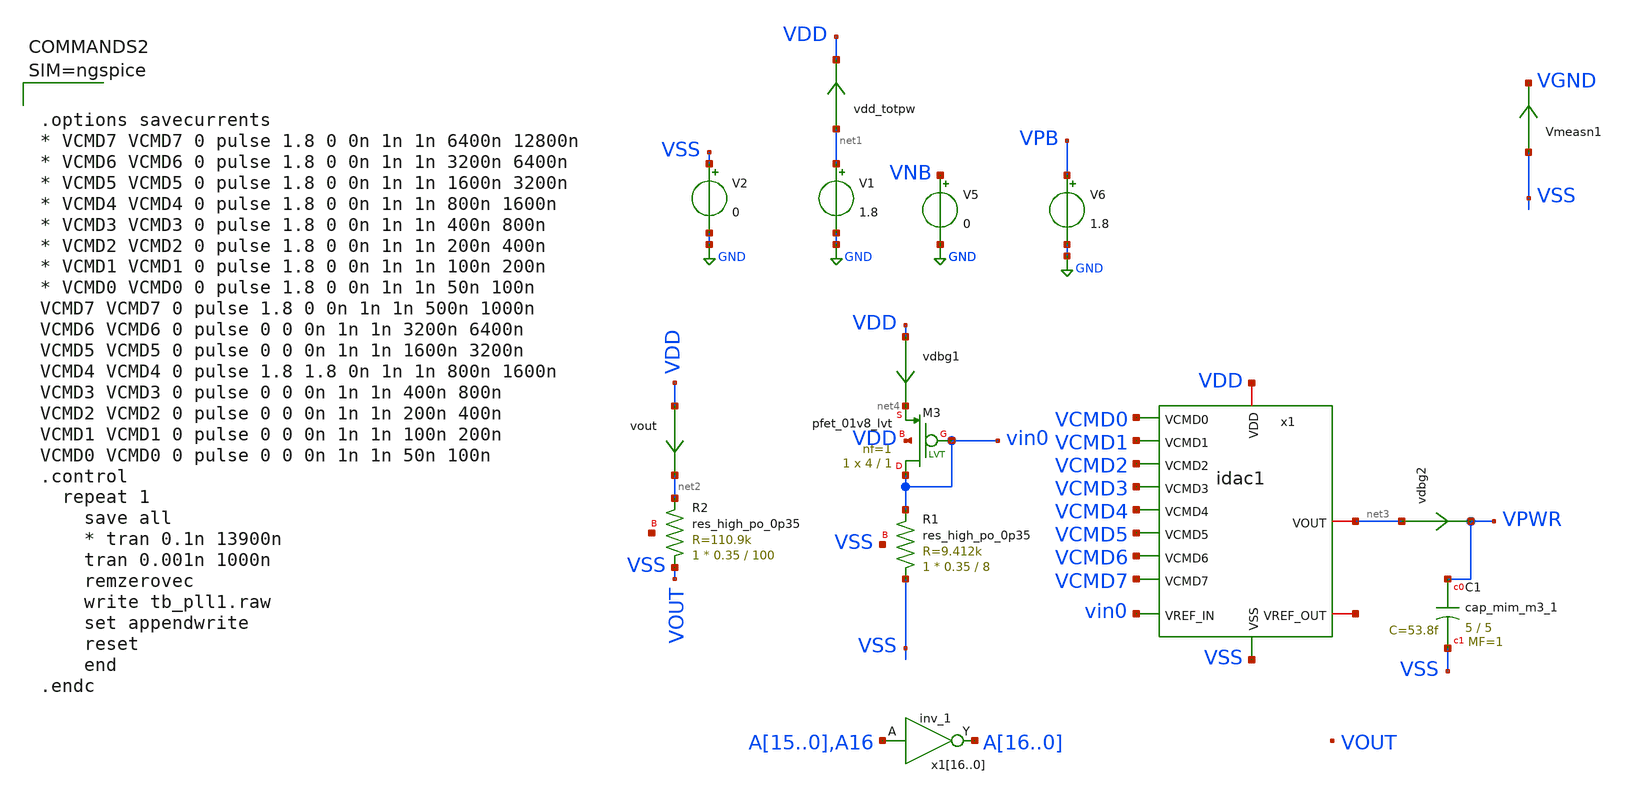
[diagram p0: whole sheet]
** sch_path: xschem/tb_pll1.sch
**.subckt tb_pll1
V5 VNB GND 0
V6 VPB GND 1.8
V1 net1 GND 1.8
V2 VSS GND 0
XM3 vin0 vin0 net4 VDD sky130_fd_pr__pfet_01v8_lvt L=1 W=4 nf=1 ad='int((nf+1)/2) * W/nf * 0.29' as='int((nf+2)/2) * W/nf * 0.29'
+ pd='2*int((nf+1)/2) * (W/nf + 0.29)' ps='2*int((nf+2)/2) * (W/nf + 0.29)' nrd='0.29 / W' nrs='0.29 / W'
+ sa=0 sb=0 sd=0 mult=1 m=1
vout VDD net2 0
.save i(vout)
XR1 VSS vin0 VSS sky130_fd_pr__res_high_po_0p35 L=8 mult=1 m=1
vdbg1 VDD net4 0
.save i(vdbg1)
XR2 VOUT net2 net5 sky130_fd_pr__res_high_po_0p35 L=100 mult=1 m=1
vdd_totpw net1 VDD 0
.save i(vdd_totpw)
x1 VCMD0 VCMD1 VCMD2 VCMD3 VCMD4 VCMD5 VCMD6 VCMD7 VDD net3 vin0 VSS net6 idac1
x116 A15 VGND VNB VPB VPWR A16 sky130_fd_sc_hd__inv_1
x115 A14 VGND VNB VPB VPWR A15 sky130_fd_sc_hd__inv_1
x114 A13 VGND VNB VPB VPWR A14 sky130_fd_sc_hd__inv_1
x113 A12 VGND VNB VPB VPWR A13 sky130_fd_sc_hd__inv_1
x112 A11 VGND VNB VPB VPWR A12 sky130_fd_sc_hd__inv_1
x111 A10 VGND VNB VPB VPWR A11 sky130_fd_sc_hd__inv_1
x110 A9 VGND VNB VPB VPWR A10 sky130_fd_sc_hd__inv_1
x19 A8 VGND VNB VPB VPWR A9 sky130_fd_sc_hd__inv_1
x18 A7 VGND VNB VPB VPWR A8 sky130_fd_sc_hd__inv_1
x17 A6 VGND VNB VPB VPWR A7 sky130_fd_sc_hd__inv_1
x16 A5 VGND VNB VPB VPWR A6 sky130_fd_sc_hd__inv_1
x15 A4 VGND VNB VPB VPWR A5 sky130_fd_sc_hd__inv_1
x14 A3 VGND VNB VPB VPWR A4 sky130_fd_sc_hd__inv_1
x13 A2 VGND VNB VPB VPWR A3 sky130_fd_sc_hd__inv_1
x12 A1 VGND VNB VPB VPWR A2 sky130_fd_sc_hd__inv_1
x11 A0 VGND VNB VPB VPWR A1 sky130_fd_sc_hd__inv_1
x10 A16 VGND VNB VPB VPWR A0 sky130_fd_sc_hd__inv_1
Vmeasn1 VSS VGND 0
.save i(vmeasn1)
vdbg2 net3 VPWR 0
.save i(vdbg2)
XC1 VPWR VSS sky130_fd_pr__cap_mim_m3_1 W=5 L=5 MF=1 m=1
**** begin user architecture code

** opencircuitdesign pdks install
.lib $::SKYWATER_MODELS/sky130.lib.spice tt_mm
*.lib $::SKYWATER_STDCELLS/sky130_fd_sc_hd_blablabla.spice

.subckt sky130_fd_sc_hd__inv_1 A VGND VNB VPB VPWR Y
X0 VGND A Y VNB sky130_fd_pr__nfet_01v8 w=650000u l=150000u
X1 VPWR A Y VPB sky130_fd_pr__pfet_01v8_hvt w=1e+06u l=150000u
.ends





.options savecurrents
* VCMD7 VCMD7 0 pulse 1.8 0 0n 1n 1n 6400n 12800n
* VCMD6 VCMD6 0 pulse 1.8 0 0n 1n 1n 3200n 6400n
* VCMD5 VCMD5 0 pulse 1.8 0 0n 1n 1n 1600n 3200n
* VCMD4 VCMD4 0 pulse 1.8 0 0n 1n 1n 800n 1600n
* VCMD3 VCMD3 0 pulse 1.8 0 0n 1n 1n 400n 800n
* VCMD2 VCMD2 0 pulse 1.8 0 0n 1n 1n 200n 400n
* VCMD1 VCMD1 0 pulse 1.8 0 0n 1n 1n 100n 200n
* VCMD0 VCMD0 0 pulse 1.8 0 0n 1n 1n 50n 100n
VCMD7 VCMD7 0 pulse 1.8 0 0n 1n 1n 500n 1000n
VCMD6 VCMD6 0 pulse 0 0 0n 1n 1n 3200n 6400n
VCMD5 VCMD5 0 pulse 0 0 0n 1n 1n 1600n 3200n
VCMD4 VCMD4 0 pulse 1.8 1.8 0n 1n 1n 800n 1600n
VCMD3 VCMD3 0 pulse 0 0 0n 1n 1n 400n 800n
VCMD2 VCMD2 0 pulse 0 0 0n 1n 1n 200n 400n
VCMD1 VCMD1 0 pulse 0 0 0n 1n 1n 100n 200n
VCMD0 VCMD0 0 pulse 0 0 0n 1n 1n 50n 100n
.control
  repeat 1
    save all
    * tran 0.1n 13900n
    tran 0.001n 1000n
    remzerovec
    write tb_pll1.raw
    set appendwrite
    reset
    end
.endc



**** end user architecture code
**.ends

* expanding   symbol:  idac1.sym # of pins=13
** sym_path: xschem/idac1.sym
** sch_path: xschem/idac1.sch
.subckt idac1 VCMD0 VCMD1 VCMD2 VCMD3 VCMD4 VCMD5 VCMD6 VCMD7 VDD VOUT VREF_IN VSS VREF_OUT
*.ipin VSS
*.iopin VREF_IN
*.iopin VOUT
*.iopin VDD
*.ipin VCMD7
*.ipin VCMD6
*.ipin VCMD5
*.ipin VCMD4
*.ipin VCMD3
*.ipin VCMD2
*.ipin VCMD1
*.ipin VCMD0
*.iopin VREF_OUT
xcell7 vin6 vin7 VOUT VDD VSS VCMD0 idac1cell
xcell6 vin5 vin6 VOUT VDD VSS VCMD1 idac1cell
xcell5 vin4 vin5 VOUT VDD VSS VCMD2 idac1cell
xcell4 vin3 vin4 VOUT VDD VSS VCMD3 idac1cell
xcell3 vin2 vin3 VOUT VDD VSS VCMD4 idac1cell
xcell2 vin1 vin2 VOUT VDD VSS VCMD5 idac1cell
xcell1 vin0 vin1 VOUT VDD VSS VCMD6 idac1cell
xcell0 VREF_IN vin0 VOUT VDD VSS VCMD7 idac1cell
.ends


* expanding   symbol:  idac1cell.sym # of pins=6
** sym_path: idac1cell.sym
** sch_path: idac1cell.sch
.subckt idac1cell VREF_IN VREF_OUT IOUT VDD VSS OE
*.ipin VSS
*.iopin VREF_OUT
*.ipin VREF_IN
*.iopin VDD
*.iopin IOUT
*.ipin OE
XM25 net1 net1 net2 net2 sky130_fd_pr__nfet_01v8_lvt L=1 W=2 nf=1 ad='int((nf+1)/2) * W/nf * 0.29' as='int((nf+2)/2) * W/nf * 0.29'
+ pd='2*int((nf+1)/2) * (W/nf + 0.29)' ps='2*int((nf+2)/2) * (W/nf + 0.29)' nrd='0.29 / W' nrs='0.29 / W'
+ sa=0 sb=0 sd=0 mult=1 m=1
XM26 net1 net1 VSS VSS sky130_fd_pr__nfet_01v8_lvt L=1 W=2 nf=1 ad='int((nf+1)/2) * W/nf * 0.29' as='int((nf+2)/2) * W/nf * 0.29'
+ pd='2*int((nf+1)/2) * (W/nf + 0.29)' ps='2*int((nf+2)/2) * (W/nf + 0.29)' nrd='0.29 / W' nrs='0.29 / W'
+ sa=0 sb=0 sd=0 mult=1 m=1
XM27 net1 VREF_IN VDD VDD sky130_fd_pr__pfet_01v8_lvt L=1 W=4 nf=1 ad='int((nf+1)/2) * W/nf * 0.29' as='int((nf+2)/2) * W/nf * 0.29'
+ pd='2*int((nf+1)/2) * (W/nf + 0.29)' ps='2*int((nf+2)/2) * (W/nf + 0.29)' nrd='0.29 / W' nrs='0.29 / W'
+ sa=0 sb=0 sd=0 mult=1 m=1
XM28 net3 net1 VSS VSS sky130_fd_pr__nfet_01v8_lvt L=1 W=2 nf=1 ad='int((nf+1)/2) * W/nf * 0.29' as='int((nf+2)/2) * W/nf * 0.29'
+ pd='2*int((nf+1)/2) * (W/nf + 0.29)' ps='2*int((nf+2)/2) * (W/nf + 0.29)' nrd='0.29 / W' nrs='0.29 / W'
+ sa=0 sb=0 sd=0 mult=1 m=1
XM29 VREF_OUT VREF_OUT VDD VDD sky130_fd_pr__pfet_01v8_lvt L=1 W=4 nf=1 ad='int((nf+1)/2) * W/nf * 0.29'
+ as='int((nf+2)/2) * W/nf * 0.29' pd='2*int((nf+1)/2) * (W/nf + 0.29)' ps='2*int((nf+2)/2) * (W/nf + 0.29)'
+ nrd='0.29 / W' nrs='0.29 / W' sa=0 sb=0 sd=0 mult=1 m=1
XM30 vdrain2 net1 VSS VSS sky130_fd_pr__nfet_01v8_lvt L=1 W=2 nf=1 ad='int((nf+1)/2) * W/nf * 0.29' as='int((nf+2)/2) * W/nf * 0.29'
+ pd='2*int((nf+1)/2) * (W/nf + 0.29)' ps='2*int((nf+2)/2) * (W/nf + 0.29)' nrd='0.29 / W' nrs='0.29 / W'
+ sa=0 sb=0 sd=0 mult=1 m=1
XM31 net4 OE vdrain2 VSS sky130_fd_pr__nfet_01v8_lvt L=1 W=2 nf=1 ad='int((nf+1)/2) * W/nf * 0.29' as='int((nf+2)/2) * W/nf * 0.29'
+ pd='2*int((nf+1)/2) * (W/nf + 0.29)' ps='2*int((nf+2)/2) * (W/nf + 0.29)' nrd='0.29 / W' nrs='0.29 / W'
+ sa=0 sb=0 sd=0 mult=1 m=1
vref net2 VSS 0
.save i(vref)
vmeas VREF_OUT net3 0
.save i(vmeas)
viout IOUT net4 0
.save i(viout)
.ends

.GLOBAL GND
.end
